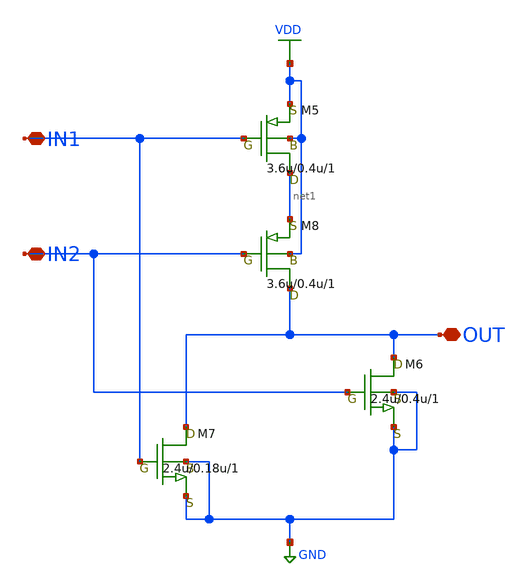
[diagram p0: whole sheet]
** sch_path: LR_hasegawa/LR_Work2/Citizen035/NOR2_Citizen.sch
**.subckt NOR2_Citizen IN2 IN1 OUT
*.iopin IN2
*.iopin IN1
*.iopin OUT
M5 net1 IN1 VDD VDD pch w=3.6u l=0.4u as=0 ps=0 ad=0 pd=0 m=1
M6 OUT IN2 GND GND nch w=2.4u l=0.4u as=0 ps=0 ad=0 pd=0 m=1
M7 OUT IN1 GND GND nch w=2.4u l=0.18u as=0 ps=0 ad=0 pd=0 m=1
M8 OUT IN2 net1 VDD pch w=3.6u l=0.4u as=0 ps=0 ad=0 pd=0 m=1
**.ends
.GLOBAL VDD
.GLOBAL GND
.end
